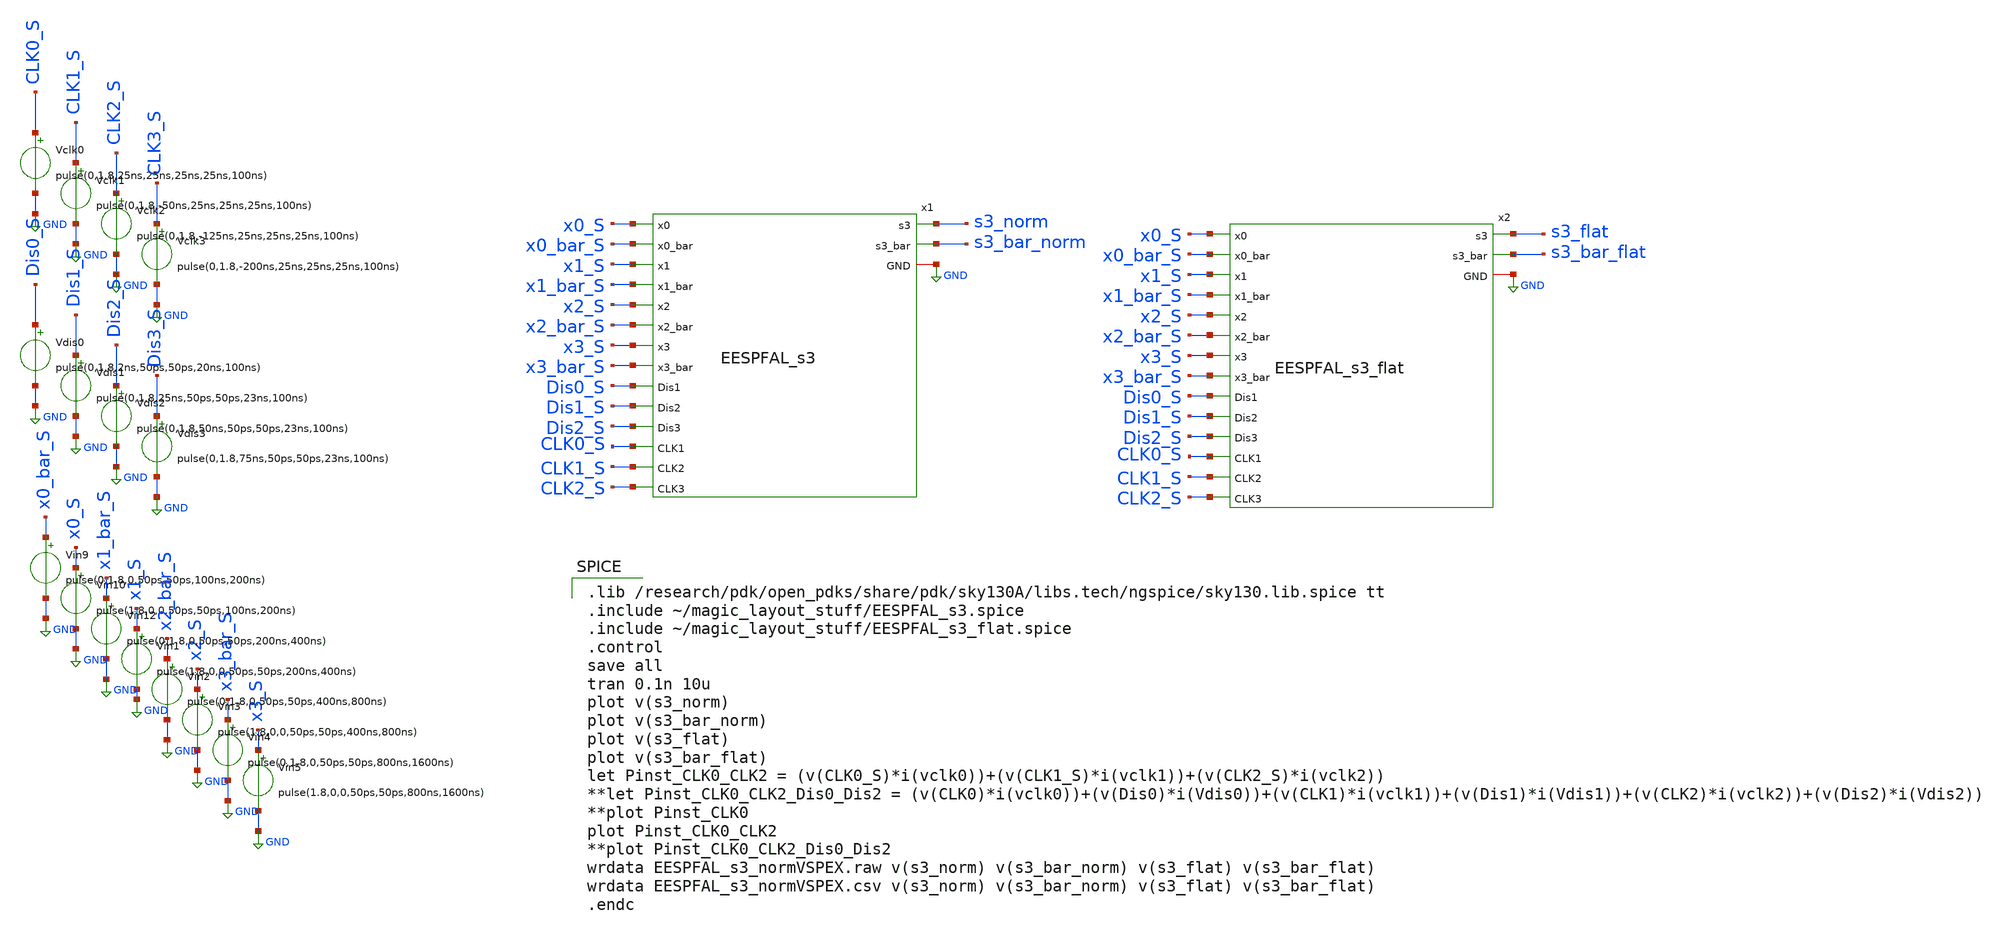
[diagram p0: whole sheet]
** sch_path: skywater_stuff/EESPFAL_s3_sim.sch
**.subckt EESPFAL_s3_sim
Vin9 x0_bar_S GND pulse(0,1.8,0,50ps,50ps,100ns,200ns)
Vin10 x0_S GND pulse(1.8,0,0,50ps,50ps,100ns,200ns)
Vin12 x1_bar_S GND pulse(0,1.8,0,50ps,50ps,200ns,400ns)
Vin1 x1_S GND pulse(1.8,0,0,50ps,50ps,200ns,400ns)
Vin2 x2_bar_S GND pulse(0,1.8,0,50ps,50ps,400ns,800ns)
Vin3 x2_S GND pulse(1.8,0,0,50ps,50ps,400ns,800ns)
Vin4 x3_bar_S GND pulse(0,1.8,0,50ps,50ps,800ns,1600ns)
Vin5 x3_S GND pulse(1.8,0,0,50ps,50ps,800ns,1600ns)
Vdis0 Dis0_S GND pulse(0,1.8,2ns,50ps,50ps,20ns,100ns)
Vclk0 CLK0_S GND pulse(0,1.8,25ns,25ns,25ns,25ns,100ns)
Vdis1 Dis1_S GND pulse(0,1.8,25ns,50ps,50ps,23ns,100ns)
Vdis2 Dis2_S GND pulse(0,1.8,50ns,50ps,50ps,23ns,100ns)
Vdis3 Dis3_S GND pulse(0,1.8,75ns,50ps,50ps,23ns,100ns)
Vclk1 CLK1_S GND pulse(0,1.8,-50ns,25ns,25ns,25ns,100ns)
Vclk2 CLK2_S GND pulse(0,1.8,-125ns,25ns,25ns,25ns,100ns)
Vclk3 CLK3_S GND pulse(0,1.8,-200ns,25ns,25ns,25ns,100ns)
x1 GND x0_S x0_bar_S x1_S x1_bar_S x2_S x2_bar_S x3_S x3_bar_S s3_bar_norm CLK0_S s3_norm Dis0_S
+ Dis2_S CLK2_S Dis1_S CLK1_S EESPFAL_s3
x2 GND x0_S x0_bar_S x1_S x1_bar_S x2_S x2_bar_S x3_S x3_bar_S s3_bar_flat s3_flat Dis0_S Dis2_S
+ Dis1_S CLK0_S CLK1_S CLK2_S EESPFAL_s3_flat
**** begin user architecture code

.lib /research/pdk/open_pdks/share/pdk/sky130A/libs.tech/ngspice/sky130.lib.spice tt
.include ~/magic_layout_stuff/EESPFAL_s3.spice
.include ~/magic_layout_stuff/EESPFAL_s3_flat.spice
.control
save all
tran 0.1n 10u
plot v(s3_norm)
plot v(s3_bar_norm)
plot v(s3_flat)
plot v(s3_bar_flat)
let Pinst_CLK0_CLK2 = (v(CLK0_S)*i(vclk0))+(v(CLK1_S)*i(vclk1))+(v(CLK2_S)*i(vclk2))
**let Pinst_CLK0_CLK2_Dis0_Dis2 =
*+ (v(CLK0)*i(vclk0))+(v(Dis0)*i(Vdis0))+(v(CLK1)*i(vclk1))+(v(Dis1)*i(Vdis1))+(v(CLK2)*i(vclk2))+(v(Dis2)*i(Vdis2))
**plot Pinst_CLK0
plot Pinst_CLK0_CLK2
**plot Pinst_CLK0_CLK2_Dis0_Dis2
wrdata EESPFAL_s3_normVSPEX.raw v(s3_norm) v(s3_bar_norm) v(s3_flat) v(s3_bar_flat)
wrdata EESPFAL_s3_normVSPEX.csv v(s3_norm) v(s3_bar_norm) v(s3_flat) v(s3_bar_flat)
.endc


**** end user architecture code
**.ends
.GLOBAL GND
.end
